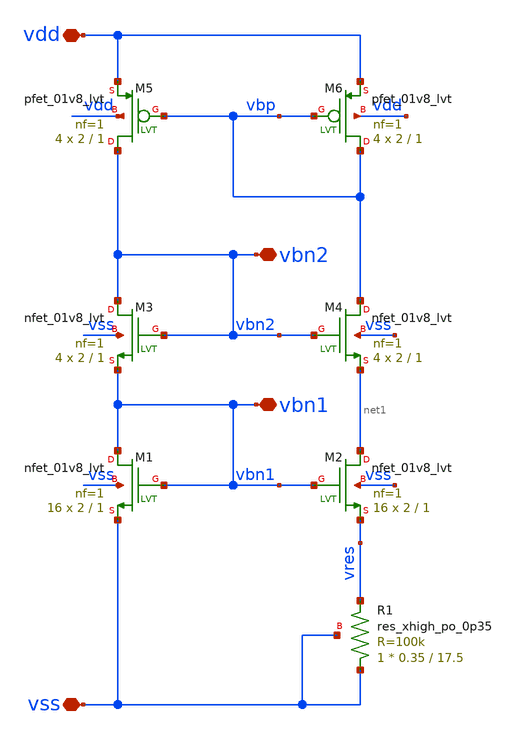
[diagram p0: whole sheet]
** sch_path: xschem/bias/bias_const_gm.sch
**.subckt bias_const_gm vbn2 vbn1 vdd vss
*.iopin vbn2
*.iopin vbn1
*.iopin vdd
*.iopin vss
XM3 vbn2 vbn2 vbn1 vss sky130_fd_pr__nfet_01v8_lvt L=1 W=2 nf=1 ad='int((nf+1)/2) * W/nf * 0.29' as='int((nf+2)/2) * W/nf * 0.29'
+ pd='2*int((nf+1)/2) * (W/nf + 0.29)' ps='2*int((nf+2)/2) * (W/nf + 0.29)' nrd='0.29 / W' nrs='0.29 / W'
+ sa=0 sb=0 sd=0 mult=4 m=4
XM4 vbp vbn2 net1 vss sky130_fd_pr__nfet_01v8_lvt L=1 W=2 nf=1 ad='int((nf+1)/2) * W/nf * 0.29' as='int((nf+2)/2) * W/nf * 0.29'
+ pd='2*int((nf+1)/2) * (W/nf + 0.29)' ps='2*int((nf+2)/2) * (W/nf + 0.29)' nrd='0.29 / W' nrs='0.29 / W'
+ sa=0 sb=0 sd=0 mult=4 m=4
XM6 vbp vbp vdd vdd sky130_fd_pr__pfet_01v8_lvt L=1 W=2 nf=1 ad='int((nf+1)/2) * W/nf * 0.29' as='int((nf+2)/2) * W/nf * 0.29'
+ pd='2*int((nf+1)/2) * (W/nf + 0.29)' ps='2*int((nf+2)/2) * (W/nf + 0.29)' nrd='0.29 / W' nrs='0.29 / W'
+ sa=0 sb=0 sd=0 mult=4 m=4
XM5 vbn2 vbp vdd vdd sky130_fd_pr__pfet_01v8_lvt L=1 W=2 nf=1 ad='int((nf+1)/2) * W/nf * 0.29' as='int((nf+2)/2) * W/nf * 0.29'
+ pd='2*int((nf+1)/2) * (W/nf + 0.29)' ps='2*int((nf+2)/2) * (W/nf + 0.29)' nrd='0.29 / W' nrs='0.29 / W'
+ sa=0 sb=0 sd=0 mult=4 m=4
XM1 vbn1 vbn1 vss vss sky130_fd_pr__nfet_01v8_lvt L=1 W=2 nf=1 ad='int((nf+1)/2) * W/nf * 0.29' as='int((nf+2)/2) * W/nf * 0.29'
+ pd='2*int((nf+1)/2) * (W/nf + 0.29)' ps='2*int((nf+2)/2) * (W/nf + 0.29)' nrd='0.29 / W' nrs='0.29 / W'
+ sa=0 sb=0 sd=0 mult=16 m=16
XM2 net1 vbn1 vres vss sky130_fd_pr__nfet_01v8_lvt L=1 W=2 nf=1 ad='int((nf+1)/2) * W/nf * 0.29' as='int((nf+2)/2) * W/nf * 0.29'
+ pd='2*int((nf+1)/2) * (W/nf + 0.29)' ps='2*int((nf+2)/2) * (W/nf + 0.29)' nrd='0.29 / W' nrs='0.29 / W'
+ sa=0 sb=0 sd=0 mult=16 m=16
XR1 vss vres vss sky130_fd_pr__res_xhigh_po_0p35 L=17.5 mult=1 m=1
**.ends
.end
